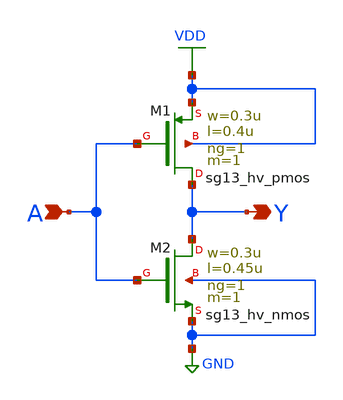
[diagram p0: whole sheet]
** sch_path: 3_real_circuits/inverter.sch
**.subckt inverter Y A
*.opin Y
*.ipin A
XM2 Y A GND GND sg13_hv_nmos w=0.3u l=0.45u ng=1 m=1 mm_ok=1
XM1 Y A VDD VDD sg13_hv_pmos w=0.3u l=0.4u ng=1 m=1 mm_ok=1
**.ends
.GLOBAL GND
.GLOBAL VDD
.end
